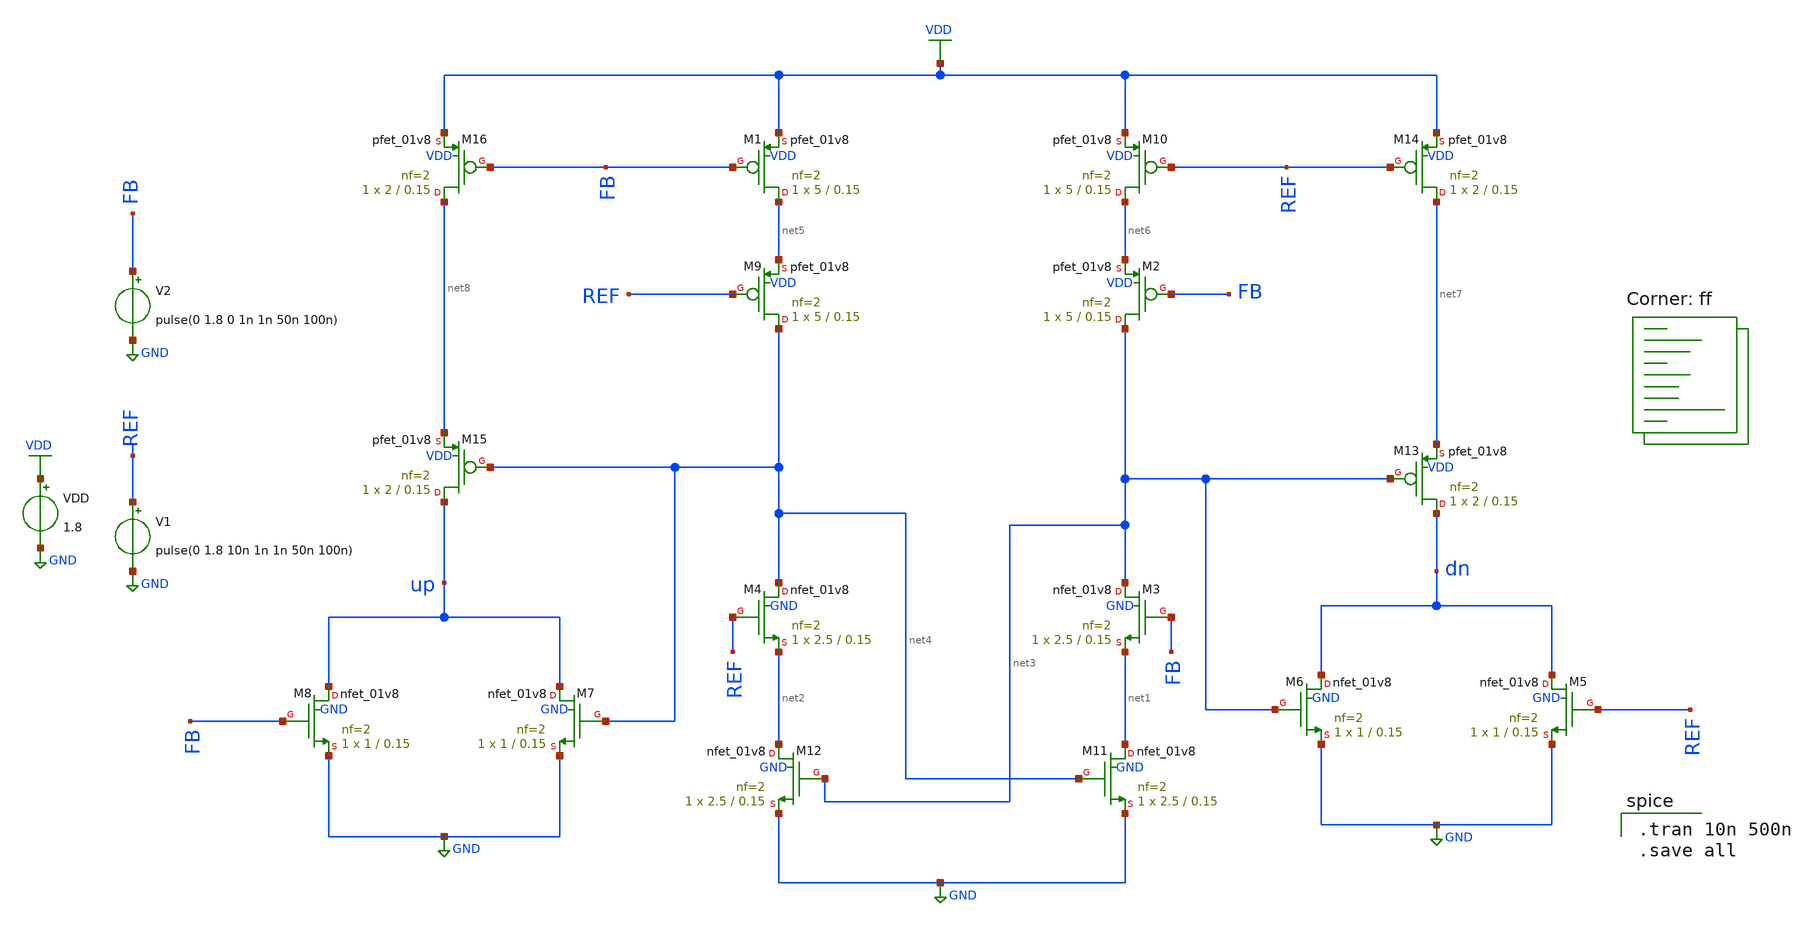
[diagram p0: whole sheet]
** sch_path: pll/pfd_cp_lf_lib/PFD/xschem/PFD.sch
**.subckt PFD
VDD VDD GND 1.8
V1 REF GND pulse(0 1.8 10n 1n 1n 50n 100n)
V2 FB GND pulse(0 1.8 0 1n 1n 50n 100n)
XM3 net3 FB net1 GND sky130_fd_pr__nfet_01v8 L=0.15 W=2.5 nf=2 ad='int((nf+1)/2) * W/nf * 0.29' as='int((nf+2)/2) * W/nf * 0.29'
+ pd='2*int((nf+1)/2) * (W/nf + 0.29)' ps='2*int((nf+2)/2) * (W/nf + 0.29)' nrd='0.29 / W' nrs='0.29 / W'
+ sa=0 sb=0 sd=0 mult=1 m=1
XM4 net4 REF net2 GND sky130_fd_pr__nfet_01v8 L=0.15 W=2.5 nf=2 ad='int((nf+1)/2) * W/nf * 0.29' as='int((nf+2)/2) * W/nf * 0.29'
+ pd='2*int((nf+1)/2) * (W/nf + 0.29)' ps='2*int((nf+2)/2) * (W/nf + 0.29)' nrd='0.29 / W' nrs='0.29 / W'
+ sa=0 sb=0 sd=0 mult=1 m=1
XM5 dn REF GND GND sky130_fd_pr__nfet_01v8 L=0.15 W=1 nf=2 ad='int((nf+1)/2) * W/nf * 0.29' as='int((nf+2)/2) * W/nf * 0.29'
+ pd='2*int((nf+1)/2) * (W/nf + 0.29)' ps='2*int((nf+2)/2) * (W/nf + 0.29)' nrd='0.29 / W' nrs='0.29 / W'
+ sa=0 sb=0 sd=0 mult=1 m=1
XM6 dn net3 GND GND sky130_fd_pr__nfet_01v8 L=0.15 W=1 nf=2 ad='int((nf+1)/2) * W/nf * 0.29' as='int((nf+2)/2) * W/nf * 0.29'
+ pd='2*int((nf+1)/2) * (W/nf + 0.29)' ps='2*int((nf+2)/2) * (W/nf + 0.29)' nrd='0.29 / W' nrs='0.29 / W'
+ sa=0 sb=0 sd=0 mult=1 m=1
XM7 up net4 GND GND sky130_fd_pr__nfet_01v8 L=0.15 W=1 nf=2 ad='int((nf+1)/2) * W/nf * 0.29' as='int((nf+2)/2) * W/nf * 0.29'
+ pd='2*int((nf+1)/2) * (W/nf + 0.29)' ps='2*int((nf+2)/2) * (W/nf + 0.29)' nrd='0.29 / W' nrs='0.29 / W'
+ sa=0 sb=0 sd=0 mult=1 m=1
XM8 up FB GND GND sky130_fd_pr__nfet_01v8 L=0.15 W=1 nf=2 ad='int((nf+1)/2) * W/nf * 0.29' as='int((nf+2)/2) * W/nf * 0.29'
+ pd='2*int((nf+1)/2) * (W/nf + 0.29)' ps='2*int((nf+2)/2) * (W/nf + 0.29)' nrd='0.29 / W' nrs='0.29 / W'
+ sa=0 sb=0 sd=0 mult=1 m=1
XM9 net4 REF net5 VDD sky130_fd_pr__pfet_01v8 L=0.15 W=5 nf=2 ad='int((nf+1)/2) * W/nf * 0.29' as='int((nf+2)/2) * W/nf * 0.29'
+ pd='2*int((nf+1)/2) * (W/nf + 0.29)' ps='2*int((nf+2)/2) * (W/nf + 0.29)' nrd='0.29 / W' nrs='0.29 / W'
+ sa=0 sb=0 sd=0 mult=1 m=1
XM1 net5 FB VDD VDD sky130_fd_pr__pfet_01v8 L=0.15 W=5 nf=2 ad='int((nf+1)/2) * W/nf * 0.29' as='int((nf+2)/2) * W/nf * 0.29'
+ pd='2*int((nf+1)/2) * (W/nf + 0.29)' ps='2*int((nf+2)/2) * (W/nf + 0.29)' nrd='0.29 / W' nrs='0.29 / W'
+ sa=0 sb=0 sd=0 mult=1 m=1
XM2 net3 FB net6 VDD sky130_fd_pr__pfet_01v8 L=0.15 W=5 nf=2 ad='int((nf+1)/2) * W/nf * 0.29' as='int((nf+2)/2) * W/nf * 0.29'
+ pd='2*int((nf+1)/2) * (W/nf + 0.29)' ps='2*int((nf+2)/2) * (W/nf + 0.29)' nrd='0.29 / W' nrs='0.29 / W'
+ sa=0 sb=0 sd=0 mult=1 m=1
XM10 net6 REF VDD VDD sky130_fd_pr__pfet_01v8 L=0.15 W=5 nf=2 ad='int((nf+1)/2) * W/nf * 0.29' as='int((nf+2)/2) * W/nf * 0.29'
+ pd='2*int((nf+1)/2) * (W/nf + 0.29)' ps='2*int((nf+2)/2) * (W/nf + 0.29)' nrd='0.29 / W' nrs='0.29 / W'
+ sa=0 sb=0 sd=0 mult=1 m=1
XM13 dn net3 net7 VDD sky130_fd_pr__pfet_01v8 L=0.15 W=2 nf=2 ad='int((nf+1)/2) * W/nf * 0.29' as='int((nf+2)/2) * W/nf * 0.29'
+ pd='2*int((nf+1)/2) * (W/nf + 0.29)' ps='2*int((nf+2)/2) * (W/nf + 0.29)' nrd='0.29 / W' nrs='0.29 / W'
+ sa=0 sb=0 sd=0 mult=1 m=1
XM14 net7 REF VDD VDD sky130_fd_pr__pfet_01v8 L=0.15 W=2 nf=2 ad='int((nf+1)/2) * W/nf * 0.29' as='int((nf+2)/2) * W/nf * 0.29'
+ pd='2*int((nf+1)/2) * (W/nf + 0.29)' ps='2*int((nf+2)/2) * (W/nf + 0.29)' nrd='0.29 / W' nrs='0.29 / W'
+ sa=0 sb=0 sd=0 mult=1 m=1
XM15 up net4 net8 VDD sky130_fd_pr__pfet_01v8 L=0.15 W=2 nf=2 ad='int((nf+1)/2) * W/nf * 0.29' as='int((nf+2)/2) * W/nf * 0.29'
+ pd='2*int((nf+1)/2) * (W/nf + 0.29)' ps='2*int((nf+2)/2) * (W/nf + 0.29)' nrd='0.29 / W' nrs='0.29 / W'
+ sa=0 sb=0 sd=0 mult=1 m=1
XM16 net8 FB VDD VDD sky130_fd_pr__pfet_01v8 L=0.15 W=2 nf=2 ad='int((nf+1)/2) * W/nf * 0.29' as='int((nf+2)/2) * W/nf * 0.29'
+ pd='2*int((nf+1)/2) * (W/nf + 0.29)' ps='2*int((nf+2)/2) * (W/nf + 0.29)' nrd='0.29 / W' nrs='0.29 / W'
+ sa=0 sb=0 sd=0 mult=1 m=1
XM11 net1 net4 GND GND sky130_fd_pr__nfet_01v8 L=0.15 W=2.5 nf=2 ad='int((nf+1)/2) * W/nf * 0.29' as='int((nf+2)/2) * W/nf * 0.29'
+ pd='2*int((nf+1)/2) * (W/nf + 0.29)' ps='2*int((nf+2)/2) * (W/nf + 0.29)' nrd='0.29 / W' nrs='0.29 / W'
+ sa=0 sb=0 sd=0 mult=1 m=1
XM12 net2 net3 GND GND sky130_fd_pr__nfet_01v8 L=0.15 W=2.5 nf=2 ad='int((nf+1)/2) * W/nf * 0.29' as='int((nf+2)/2) * W/nf * 0.29'
+ pd='2*int((nf+1)/2) * (W/nf + 0.29)' ps='2*int((nf+2)/2) * (W/nf + 0.29)' nrd='0.29 / W' nrs='0.29 / W'
+ sa=0 sb=0 sd=0 mult=1 m=1
**** begin user architecture code
.lib $::SKYWATER_MODELS/sky130.lib.spice ff

.tran 10n 500n
.save all

**** end user architecture code
**.ends
.GLOBAL VDD
.GLOBAL GND
.end
